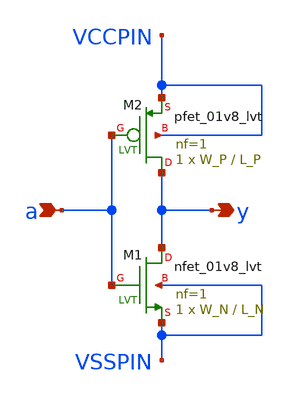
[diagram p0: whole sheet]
** sch_path: sky130A/xschem_libs/sky130_tests/lvtnot/schematic/lvtnot.sch
* Copyright 2021 Stefan Frederik Schippers
* Licensed under the Apache License, Version 2.0 (the "License");
* you may not use this file except in compliance with the License.
* You may obtain a copy of the License at
* https://www.apache.org/licenses/LICENSE-2.0
* Unless required by applicable law or agreed to in writing, software
* distributed under the License is distributed on an "AS IS" BASIS,
* WITHOUT WARRANTIES OR CONDITIONS OF ANY KIND, either express or implied.
* See the License for the specific language governing permissions and
* limitations under the License.
**.subckt lvtnot y a
*.opin y
*.ipin a
XM2 y a VCCPIN VCCPIN sky130_fd_pr__pfet_01v8_lvt L=L_P W=W_P nf=1 ad='int((1 + 1)/2) * W_P / 1 * 0.29'
+ as='int((1 + 2)/2) * W_P / 1 * 0.29' pd='2*int((1 + 1)/2) * (W_P / 1 + 0.29)' ps='2*int((1 + 2)/2) * (W_P / 1 + 0.29)'
+ nrd='0.29 / W_P ' nrs='0.29 / W_P ' sa=0 sb=0 sd=0 mult=1 m=1
XM1 y a VSSPIN VSSPIN sky130_fd_pr__nfet_01v8_lvt L=L_N W=W_N nf=1 ad='int((1 + 1)/2) * W_N / 1 * 0.29'
+ as='int((1 + 2)/2) * W_N / 1 * 0.29' pd='2*int((1 + 1)/2) * (W_N / 1 + 0.29)' ps='2*int((1 + 2)/2) * (W_N / 1 + 0.29)'
+ nrd='0.29 / W_N ' nrs='0.29 / W_N ' sa=0 sb=0 sd=0 mult=1 m=1
**.ends
.end
